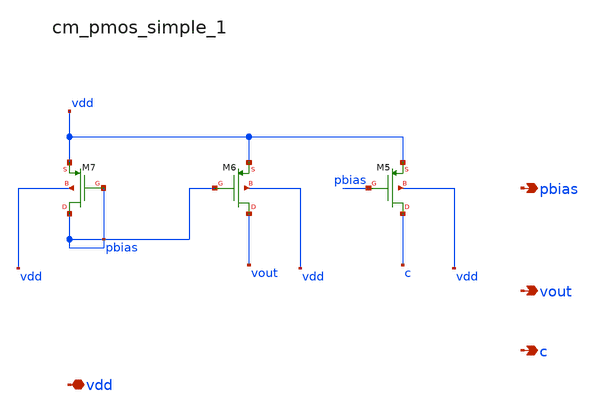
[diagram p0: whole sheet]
** sch_path: analog-db/raw/amp_022_fer_two_stage/hier/blocks/cm_pmos_simple_1.sch
**.subckt cm_pmos_simple_1 vdd pbias vout c
*.iopin vdd
*.opin pbias
*.opin vout
*.opin c
XM5 c pbias vdd vdd sg13_lv_pmos w=x_dut_xm5_w l=x_dut_xm5_l ng=1 m=x_dut_xm5_m
XM6 vout pbias vdd vdd sg13_lv_pmos w=x_dut_xm6_w l=x_dut_xm6_l ng=1 m=x_dut_xm6_m
XM7 pbias pbias vdd vdd sg13_lv_pmos w=x_dut_xm7_w l=x_dut_xm7_l ng=1 m=x_dut_xm7_m
**.ends
.end
